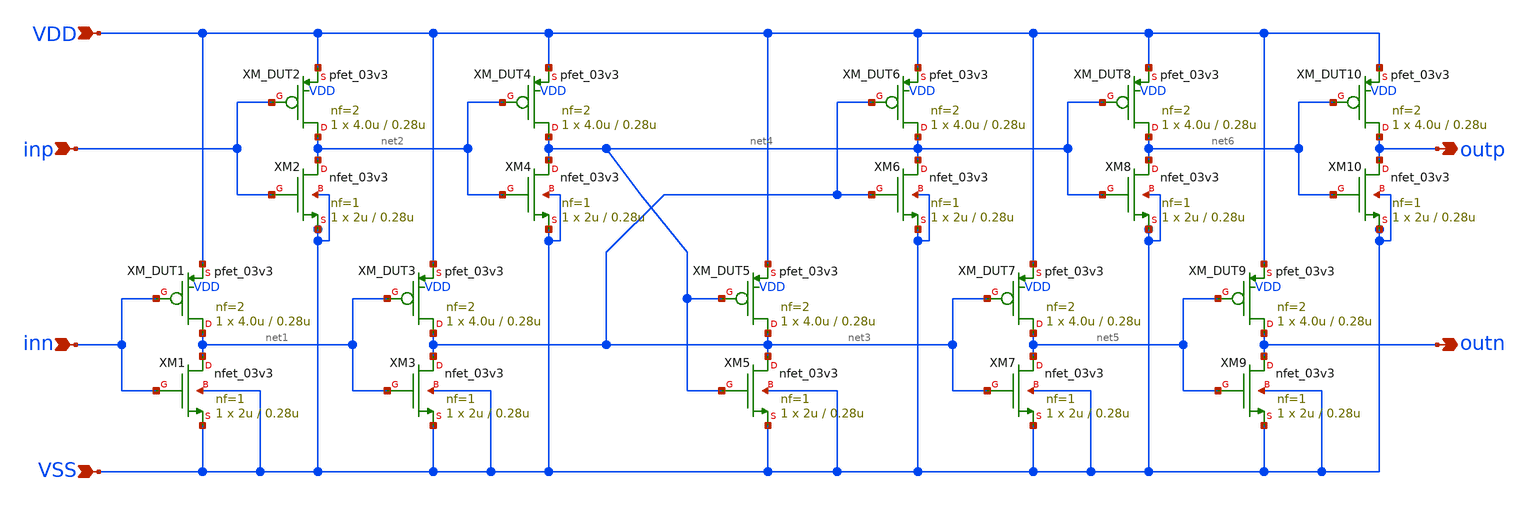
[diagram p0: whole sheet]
** sch_path: xschem/diff_buffer.sch
**.subckt diff_buffer inn outp outn VDD VSS inp
*.ipin inn
*.opin outp
*.opin outn
*.ipin VDD
*.ipin VSS
*.ipin inp
XM_DUT1 net1 inn VDD VDD pfet_03v3 L=0.28u W=4.0u nf=2 ad='int((nf+1)/2) * W/nf * 0.18u' as='int((nf+2)/2) * W/nf * 0.18u'
+ pd='2*int((nf+1)/2) * (W/nf + 0.18u)' ps='2*int((nf+2)/2) * (W/nf + 0.18u)' nrd='0.18u / W' nrs='0.18u / W'
+ sa=0 sb=0 sd=0 m=1 par=1
XM1 net1 inn VSS VSS nfet_03v3 L=0.28u W=2u nf=1 ad='int((nf+1)/2) * W/nf * 0.18u' as='int((nf+2)/2) * W/nf * 0.18u'
+ pd='2*int((nf+1)/2) * (W/nf + 0.18u)' ps='2*int((nf+2)/2) * (W/nf + 0.18u)' nrd='0.18u / W' nrs='0.18u / W'
+ sa=0 sb=0 sd=0 m=1 par=1
XM_DUT2 net2 inp VDD VDD pfet_03v3 L=0.28u W=4.0u nf=2 ad='int((nf+1)/2) * W/nf * 0.18u' as='int((nf+2)/2) * W/nf * 0.18u'
+ pd='2*int((nf+1)/2) * (W/nf + 0.18u)' ps='2*int((nf+2)/2) * (W/nf + 0.18u)' nrd='0.18u / W' nrs='0.18u / W'
+ sa=0 sb=0 sd=0 m=1 par=1
XM2 net2 inp VSS VSS nfet_03v3 L=0.28u W=2u nf=1 ad='int((nf+1)/2) * W/nf * 0.18u' as='int((nf+2)/2) * W/nf * 0.18u'
+ pd='2*int((nf+1)/2) * (W/nf + 0.18u)' ps='2*int((nf+2)/2) * (W/nf + 0.18u)' nrd='0.18u / W' nrs='0.18u / W'
+ sa=0 sb=0 sd=0 m=1 par=1
XM_DUT3 net3 net1 VDD VDD pfet_03v3 L=0.28u W=4.0u nf=2 ad='int((nf+1)/2) * W/nf * 0.18u' as='int((nf+2)/2) * W/nf * 0.18u'
+ pd='2*int((nf+1)/2) * (W/nf + 0.18u)' ps='2*int((nf+2)/2) * (W/nf + 0.18u)' nrd='0.18u / W' nrs='0.18u / W'
+ sa=0 sb=0 sd=0 m=1 par=1
XM3 net3 net1 VSS VSS nfet_03v3 L=0.28u W=2u nf=1 ad='int((nf+1)/2) * W/nf * 0.18u' as='int((nf+2)/2) * W/nf * 0.18u'
+ pd='2*int((nf+1)/2) * (W/nf + 0.18u)' ps='2*int((nf+2)/2) * (W/nf + 0.18u)' nrd='0.18u / W' nrs='0.18u / W'
+ sa=0 sb=0 sd=0 m=1 par=1
XM_DUT4 net4 net2 VDD VDD pfet_03v3 L=0.28u W=4.0u nf=2 ad='int((nf+1)/2) * W/nf * 0.18u' as='int((nf+2)/2) * W/nf * 0.18u'
+ pd='2*int((nf+1)/2) * (W/nf + 0.18u)' ps='2*int((nf+2)/2) * (W/nf + 0.18u)' nrd='0.18u / W' nrs='0.18u / W'
+ sa=0 sb=0 sd=0 m=1 par=1
XM4 net4 net2 VSS VSS nfet_03v3 L=0.28u W=2u nf=1 ad='int((nf+1)/2) * W/nf * 0.18u' as='int((nf+2)/2) * W/nf * 0.18u'
+ pd='2*int((nf+1)/2) * (W/nf + 0.18u)' ps='2*int((nf+2)/2) * (W/nf + 0.18u)' nrd='0.18u / W' nrs='0.18u / W'
+ sa=0 sb=0 sd=0 m=1 par=1
XM_DUT5 net3 net4 VDD VDD pfet_03v3 L=0.28u W=4.0u nf=2 ad='int((nf+1)/2) * W/nf * 0.18u' as='int((nf+2)/2) * W/nf * 0.18u'
+ pd='2*int((nf+1)/2) * (W/nf + 0.18u)' ps='2*int((nf+2)/2) * (W/nf + 0.18u)' nrd='0.18u / W' nrs='0.18u / W'
+ sa=0 sb=0 sd=0 m=1 par=1
XM5 net3 net4 VSS VSS nfet_03v3 L=0.28u W=2u nf=1 ad='int((nf+1)/2) * W/nf * 0.18u' as='int((nf+2)/2) * W/nf * 0.18u'
+ pd='2*int((nf+1)/2) * (W/nf + 0.18u)' ps='2*int((nf+2)/2) * (W/nf + 0.18u)' nrd='0.18u / W' nrs='0.18u / W'
+ sa=0 sb=0 sd=0 m=1 par=1
XM_DUT6 net4 net3 VDD VDD pfet_03v3 L=0.28u W=4.0u nf=2 ad='int((nf+1)/2) * W/nf * 0.18u' as='int((nf+2)/2) * W/nf * 0.18u'
+ pd='2*int((nf+1)/2) * (W/nf + 0.18u)' ps='2*int((nf+2)/2) * (W/nf + 0.18u)' nrd='0.18u / W' nrs='0.18u / W'
+ sa=0 sb=0 sd=0 m=1 par=1
XM6 net4 net3 VSS VSS nfet_03v3 L=0.28u W=2u nf=1 ad='int((nf+1)/2) * W/nf * 0.18u' as='int((nf+2)/2) * W/nf * 0.18u'
+ pd='2*int((nf+1)/2) * (W/nf + 0.18u)' ps='2*int((nf+2)/2) * (W/nf + 0.18u)' nrd='0.18u / W' nrs='0.18u / W'
+ sa=0 sb=0 sd=0 m=1 par=1
XM_DUT7 net5 net3 VDD VDD pfet_03v3 L=0.28u W=4.0u nf=2 ad='int((nf+1)/2) * W/nf * 0.18u' as='int((nf+2)/2) * W/nf * 0.18u'
+ pd='2*int((nf+1)/2) * (W/nf + 0.18u)' ps='2*int((nf+2)/2) * (W/nf + 0.18u)' nrd='0.18u / W' nrs='0.18u / W'
+ sa=0 sb=0 sd=0 m=1 par=1
XM7 net5 net3 VSS VSS nfet_03v3 L=0.28u W=2u nf=1 ad='int((nf+1)/2) * W/nf * 0.18u' as='int((nf+2)/2) * W/nf * 0.18u'
+ pd='2*int((nf+1)/2) * (W/nf + 0.18u)' ps='2*int((nf+2)/2) * (W/nf + 0.18u)' nrd='0.18u / W' nrs='0.18u / W'
+ sa=0 sb=0 sd=0 m=1 par=1
XM_DUT8 net6 net4 VDD VDD pfet_03v3 L=0.28u W=4.0u nf=2 ad='int((nf+1)/2) * W/nf * 0.18u' as='int((nf+2)/2) * W/nf * 0.18u'
+ pd='2*int((nf+1)/2) * (W/nf + 0.18u)' ps='2*int((nf+2)/2) * (W/nf + 0.18u)' nrd='0.18u / W' nrs='0.18u / W'
+ sa=0 sb=0 sd=0 m=1 par=1
XM8 net6 net4 VSS VSS nfet_03v3 L=0.28u W=2u nf=1 ad='int((nf+1)/2) * W/nf * 0.18u' as='int((nf+2)/2) * W/nf * 0.18u'
+ pd='2*int((nf+1)/2) * (W/nf + 0.18u)' ps='2*int((nf+2)/2) * (W/nf + 0.18u)' nrd='0.18u / W' nrs='0.18u / W'
+ sa=0 sb=0 sd=0 m=1 par=1
XM_DUT9 outn net5 VDD VDD pfet_03v3 L=0.28u W=4.0u nf=2 ad='int((nf+1)/2) * W/nf * 0.18u' as='int((nf+2)/2) * W/nf * 0.18u'
+ pd='2*int((nf+1)/2) * (W/nf + 0.18u)' ps='2*int((nf+2)/2) * (W/nf + 0.18u)' nrd='0.18u / W' nrs='0.18u / W'
+ sa=0 sb=0 sd=0 m=1 par=1
XM9 outn net5 VSS VSS nfet_03v3 L=0.28u W=2u nf=1 ad='int((nf+1)/2) * W/nf * 0.18u' as='int((nf+2)/2) * W/nf * 0.18u'
+ pd='2*int((nf+1)/2) * (W/nf + 0.18u)' ps='2*int((nf+2)/2) * (W/nf + 0.18u)' nrd='0.18u / W' nrs='0.18u / W'
+ sa=0 sb=0 sd=0 m=1 par=1
XM_DUT10 outp net6 VDD VDD pfet_03v3 L=0.28u W=4.0u nf=2 ad='int((nf+1)/2) * W/nf * 0.18u' as='int((nf+2)/2) * W/nf * 0.18u'
+ pd='2*int((nf+1)/2) * (W/nf + 0.18u)' ps='2*int((nf+2)/2) * (W/nf + 0.18u)' nrd='0.18u / W' nrs='0.18u / W'
+ sa=0 sb=0 sd=0 m=1 par=1
XM10 outp net6 VSS VSS nfet_03v3 L=0.28u W=2u nf=1 ad='int((nf+1)/2) * W/nf * 0.18u' as='int((nf+2)/2) * W/nf * 0.18u'
+ pd='2*int((nf+1)/2) * (W/nf + 0.18u)' ps='2*int((nf+2)/2) * (W/nf + 0.18u)' nrd='0.18u / W' nrs='0.18u / W'
+ sa=0 sb=0 sd=0 m=1 par=1
**.ends
.end
